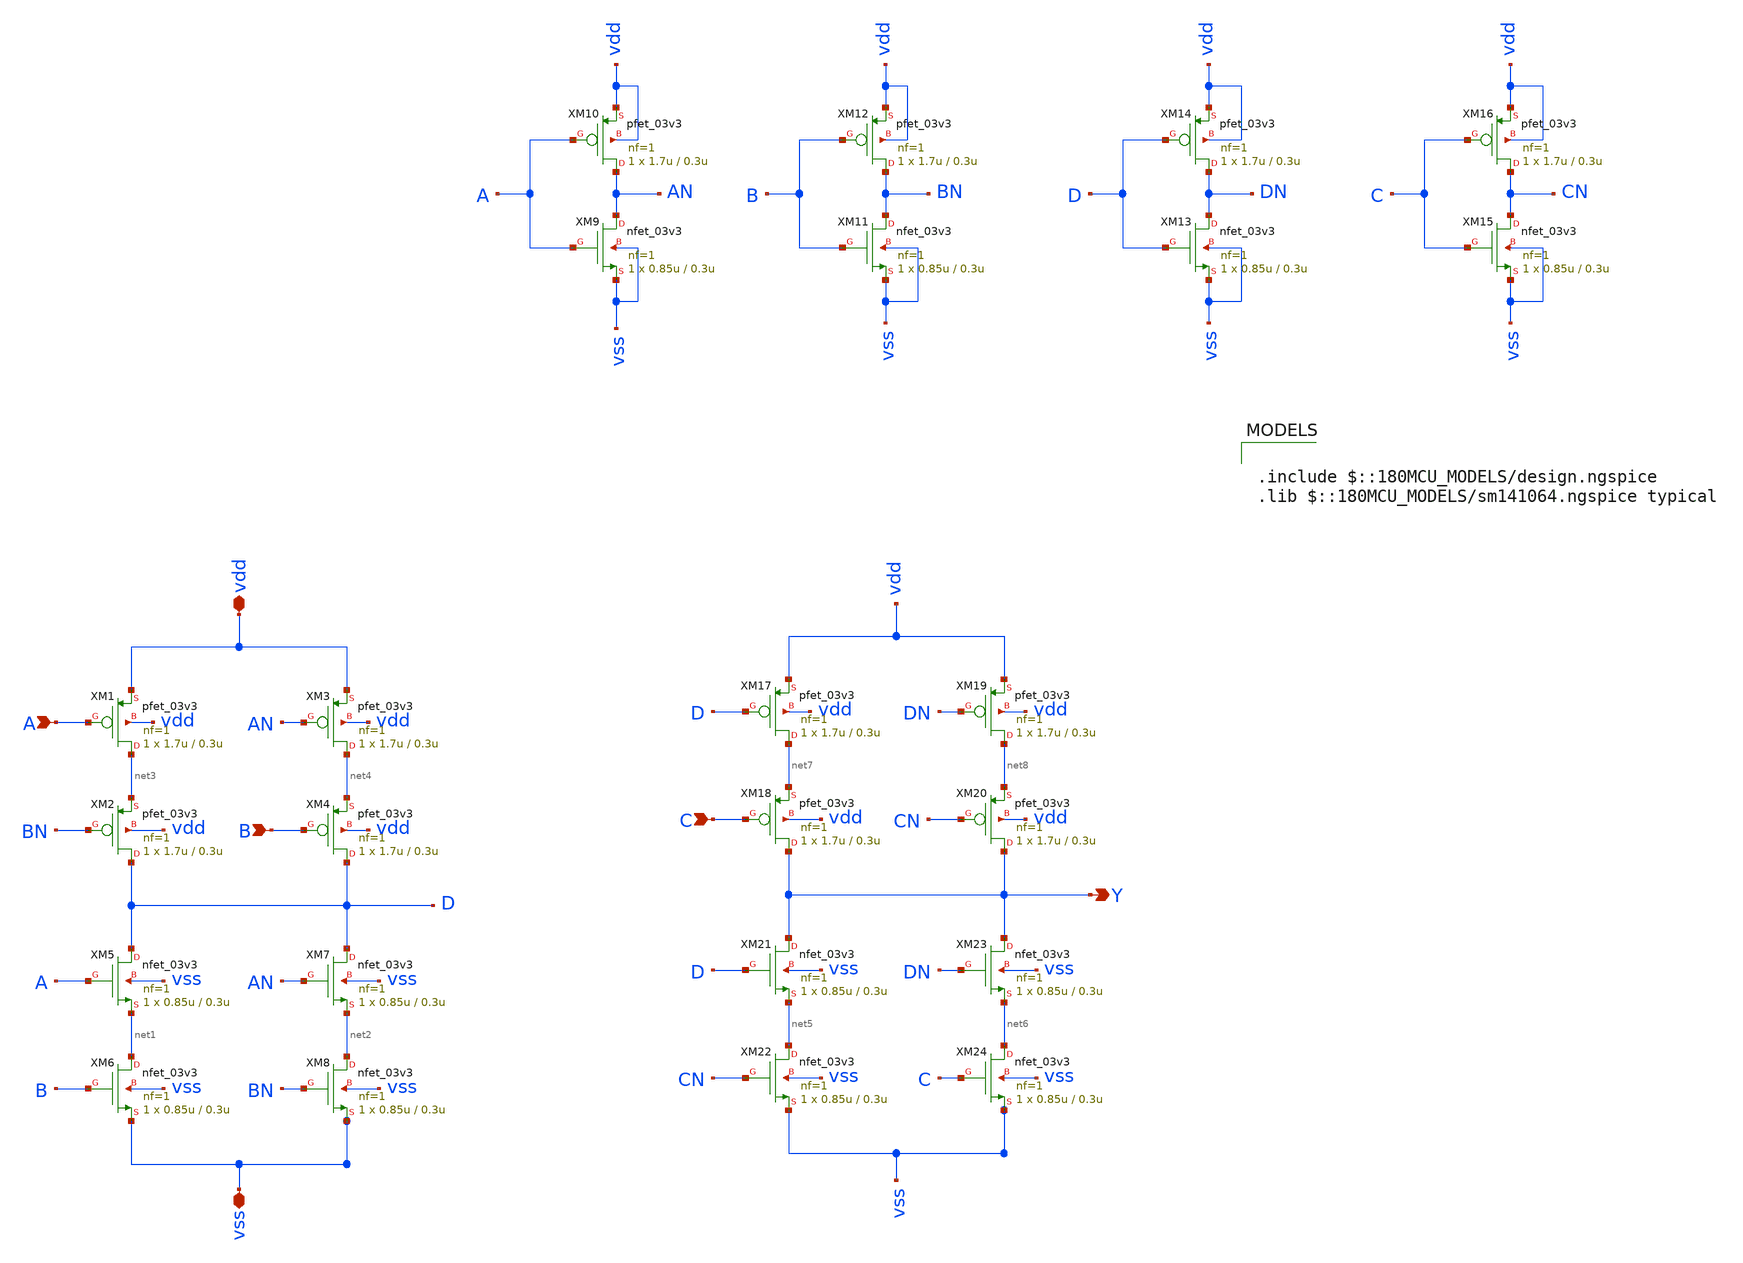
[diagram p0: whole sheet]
** sch_path: Cells/XNOR3_1/xnor3_1.sch
**.subckt xnor3_1 vss vdd A B C Y
*.iopin vss
*.iopin vdd
*.ipin A
*.ipin B
*.ipin C
*.opin Y
XM1 net3 A vdd vdd pfet_03v3 L=0.3u W=1.7u nf=1 ad='int((nf+1)/2) * W/nf * 0.18u' as='int((nf+2)/2) * W/nf * 0.18u'
+ pd='2*int((nf+1)/2) * (W/nf + 0.18u)' ps='2*int((nf+2)/2) * (W/nf + 0.18u)' nrd='0.18u / W' nrs='0.18u / W'
+ sa=0 sb=0 sd=0 m=1
XM2 D BN net3 vdd pfet_03v3 L=0.3u W=1.7u nf=1 ad='int((nf+1)/2) * W/nf * 0.18u' as='int((nf+2)/2) * W/nf * 0.18u'
+ pd='2*int((nf+1)/2) * (W/nf + 0.18u)' ps='2*int((nf+2)/2) * (W/nf + 0.18u)' nrd='0.18u / W' nrs='0.18u / W'
+ sa=0 sb=0 sd=0 m=1
XM3 net4 AN vdd vdd pfet_03v3 L=0.3u W=1.7u nf=1 ad='int((nf+1)/2) * W/nf * 0.18u' as='int((nf+2)/2) * W/nf * 0.18u'
+ pd='2*int((nf+1)/2) * (W/nf + 0.18u)' ps='2*int((nf+2)/2) * (W/nf + 0.18u)' nrd='0.18u / W' nrs='0.18u / W'
+ sa=0 sb=0 sd=0 m=1
XM4 D B net4 vdd pfet_03v3 L=0.3u W=1.7u nf=1 ad='int((nf+1)/2) * W/nf * 0.18u' as='int((nf+2)/2) * W/nf * 0.18u'
+ pd='2*int((nf+1)/2) * (W/nf + 0.18u)' ps='2*int((nf+2)/2) * (W/nf + 0.18u)' nrd='0.18u / W' nrs='0.18u / W'
+ sa=0 sb=0 sd=0 m=1
XM5 D A net1 vss nfet_03v3 L=0.3u W=0.85u nf=1 ad='int((nf+1)/2) * W/nf * 0.18u' as='int((nf+2)/2) * W/nf * 0.18u'
+ pd='2*int((nf+1)/2) * (W/nf + 0.18u)' ps='2*int((nf+2)/2) * (W/nf + 0.18u)' nrd='0.18u / W' nrs='0.18u / W'
+ sa=0 sb=0 sd=0 m=1
XM6 net1 B vss vss nfet_03v3 L=0.3u W=0.85u nf=1 ad='int((nf+1)/2) * W/nf * 0.18u' as='int((nf+2)/2) * W/nf * 0.18u'
+ pd='2*int((nf+1)/2) * (W/nf + 0.18u)' ps='2*int((nf+2)/2) * (W/nf + 0.18u)' nrd='0.18u / W' nrs='0.18u / W'
+ sa=0 sb=0 sd=0 m=1
XM7 D AN net2 vss nfet_03v3 L=0.3u W=0.85u nf=1 ad='int((nf+1)/2) * W/nf * 0.18u' as='int((nf+2)/2) * W/nf * 0.18u'
+ pd='2*int((nf+1)/2) * (W/nf + 0.18u)' ps='2*int((nf+2)/2) * (W/nf + 0.18u)' nrd='0.18u / W' nrs='0.18u / W'
+ sa=0 sb=0 sd=0 m=1
XM8 net2 BN vss vss nfet_03v3 L=0.3u W=0.85u nf=1 ad='int((nf+1)/2) * W/nf * 0.18u' as='int((nf+2)/2) * W/nf * 0.18u'
+ pd='2*int((nf+1)/2) * (W/nf + 0.18u)' ps='2*int((nf+2)/2) * (W/nf + 0.18u)' nrd='0.18u / W' nrs='0.18u / W'
+ sa=0 sb=0 sd=0 m=1
XM9 AN A vss vss nfet_03v3 L=0.3u W=0.85u nf=1 ad='int((nf+1)/2) * W/nf * 0.18u' as='int((nf+2)/2) * W/nf * 0.18u'
+ pd='2*int((nf+1)/2) * (W/nf + 0.18u)' ps='2*int((nf+2)/2) * (W/nf + 0.18u)' nrd='0.18u / W' nrs='0.18u / W'
+ sa=0 sb=0 sd=0 m=1
XM10 AN A vdd vdd pfet_03v3 L=0.3u W=1.7u nf=1 ad='int((nf+1)/2) * W/nf * 0.18u' as='int((nf+2)/2) * W/nf * 0.18u'
+ pd='2*int((nf+1)/2) * (W/nf + 0.18u)' ps='2*int((nf+2)/2) * (W/nf + 0.18u)' nrd='0.18u / W' nrs='0.18u / W'
+ sa=0 sb=0 sd=0 m=1
XM11 BN B vss vss nfet_03v3 L=0.3u W=0.85u nf=1 ad='int((nf+1)/2) * W/nf * 0.18u' as='int((nf+2)/2) * W/nf * 0.18u'
+ pd='2*int((nf+1)/2) * (W/nf + 0.18u)' ps='2*int((nf+2)/2) * (W/nf + 0.18u)' nrd='0.18u / W' nrs='0.18u / W'
+ sa=0 sb=0 sd=0 m=1
XM12 BN B vdd vdd pfet_03v3 L=0.3u W=1.7u nf=1 ad='int((nf+1)/2) * W/nf * 0.18u' as='int((nf+2)/2) * W/nf * 0.18u'
+ pd='2*int((nf+1)/2) * (W/nf + 0.18u)' ps='2*int((nf+2)/2) * (W/nf + 0.18u)' nrd='0.18u / W' nrs='0.18u / W'
+ sa=0 sb=0 sd=0 m=1
XM13 DN D vss vss nfet_03v3 L=0.3u W=0.85u nf=1 ad='int((nf+1)/2) * W/nf * 0.18u' as='int((nf+2)/2) * W/nf * 0.18u'
+ pd='2*int((nf+1)/2) * (W/nf + 0.18u)' ps='2*int((nf+2)/2) * (W/nf + 0.18u)' nrd='0.18u / W' nrs='0.18u / W'
+ sa=0 sb=0 sd=0 m=1
XM14 DN D vdd vdd pfet_03v3 L=0.3u W=1.7u nf=1 ad='int((nf+1)/2) * W/nf * 0.18u' as='int((nf+2)/2) * W/nf * 0.18u'
+ pd='2*int((nf+1)/2) * (W/nf + 0.18u)' ps='2*int((nf+2)/2) * (W/nf + 0.18u)' nrd='0.18u / W' nrs='0.18u / W'
+ sa=0 sb=0 sd=0 m=1
XM17 net7 D vdd vdd pfet_03v3 L=0.3u W=1.7u nf=1 ad='int((nf+1)/2) * W/nf * 0.18u' as='int((nf+2)/2) * W/nf * 0.18u'
+ pd='2*int((nf+1)/2) * (W/nf + 0.18u)' ps='2*int((nf+2)/2) * (W/nf + 0.18u)' nrd='0.18u / W' nrs='0.18u / W'
+ sa=0 sb=0 sd=0 m=1
XM18 Y C net7 vdd pfet_03v3 L=0.3u W=1.7u nf=1 ad='int((nf+1)/2) * W/nf * 0.18u' as='int((nf+2)/2) * W/nf * 0.18u'
+ pd='2*int((nf+1)/2) * (W/nf + 0.18u)' ps='2*int((nf+2)/2) * (W/nf + 0.18u)' nrd='0.18u / W' nrs='0.18u / W'
+ sa=0 sb=0 sd=0 m=1
XM19 net8 DN vdd vdd pfet_03v3 L=0.3u W=1.7u nf=1 ad='int((nf+1)/2) * W/nf * 0.18u' as='int((nf+2)/2) * W/nf * 0.18u'
+ pd='2*int((nf+1)/2) * (W/nf + 0.18u)' ps='2*int((nf+2)/2) * (W/nf + 0.18u)' nrd='0.18u / W' nrs='0.18u / W'
+ sa=0 sb=0 sd=0 m=1
XM20 Y CN net8 vdd pfet_03v3 L=0.3u W=1.7u nf=1 ad='int((nf+1)/2) * W/nf * 0.18u' as='int((nf+2)/2) * W/nf * 0.18u'
+ pd='2*int((nf+1)/2) * (W/nf + 0.18u)' ps='2*int((nf+2)/2) * (W/nf + 0.18u)' nrd='0.18u / W' nrs='0.18u / W'
+ sa=0 sb=0 sd=0 m=1
XM21 Y D net5 vss nfet_03v3 L=0.3u W=0.85u nf=1 ad='int((nf+1)/2) * W/nf * 0.18u' as='int((nf+2)/2) * W/nf * 0.18u'
+ pd='2*int((nf+1)/2) * (W/nf + 0.18u)' ps='2*int((nf+2)/2) * (W/nf + 0.18u)' nrd='0.18u / W' nrs='0.18u / W'
+ sa=0 sb=0 sd=0 m=1
XM22 net5 CN vss vss nfet_03v3 L=0.3u W=0.85u nf=1 ad='int((nf+1)/2) * W/nf * 0.18u' as='int((nf+2)/2) * W/nf * 0.18u'
+ pd='2*int((nf+1)/2) * (W/nf + 0.18u)' ps='2*int((nf+2)/2) * (W/nf + 0.18u)' nrd='0.18u / W' nrs='0.18u / W'
+ sa=0 sb=0 sd=0 m=1
XM23 Y DN net6 vss nfet_03v3 L=0.3u W=0.85u nf=1 ad='int((nf+1)/2) * W/nf * 0.18u' as='int((nf+2)/2) * W/nf * 0.18u'
+ pd='2*int((nf+1)/2) * (W/nf + 0.18u)' ps='2*int((nf+2)/2) * (W/nf + 0.18u)' nrd='0.18u / W' nrs='0.18u / W'
+ sa=0 sb=0 sd=0 m=1
XM24 net6 C vss vss nfet_03v3 L=0.3u W=0.85u nf=1 ad='int((nf+1)/2) * W/nf * 0.18u' as='int((nf+2)/2) * W/nf * 0.18u'
+ pd='2*int((nf+1)/2) * (W/nf + 0.18u)' ps='2*int((nf+2)/2) * (W/nf + 0.18u)' nrd='0.18u / W' nrs='0.18u / W'
+ sa=0 sb=0 sd=0 m=1
XM15 CN C vss vss nfet_03v3 L=0.3u W=0.85u nf=1 ad='int((nf+1)/2) * W/nf * 0.18u' as='int((nf+2)/2) * W/nf * 0.18u'
+ pd='2*int((nf+1)/2) * (W/nf + 0.18u)' ps='2*int((nf+2)/2) * (W/nf + 0.18u)' nrd='0.18u / W' nrs='0.18u / W'
+ sa=0 sb=0 sd=0 m=1
XM16 CN C vdd vdd pfet_03v3 L=0.3u W=1.7u nf=1 ad='int((nf+1)/2) * W/nf * 0.18u' as='int((nf+2)/2) * W/nf * 0.18u'
+ pd='2*int((nf+1)/2) * (W/nf + 0.18u)' ps='2*int((nf+2)/2) * (W/nf + 0.18u)' nrd='0.18u / W' nrs='0.18u / W'
+ sa=0 sb=0 sd=0 m=1
**** begin user architecture code

.include $::180MCU_MODELS/design.ngspice
.lib $::180MCU_MODELS/sm141064.ngspice typical

**** end user architecture code
**.ends
.end
